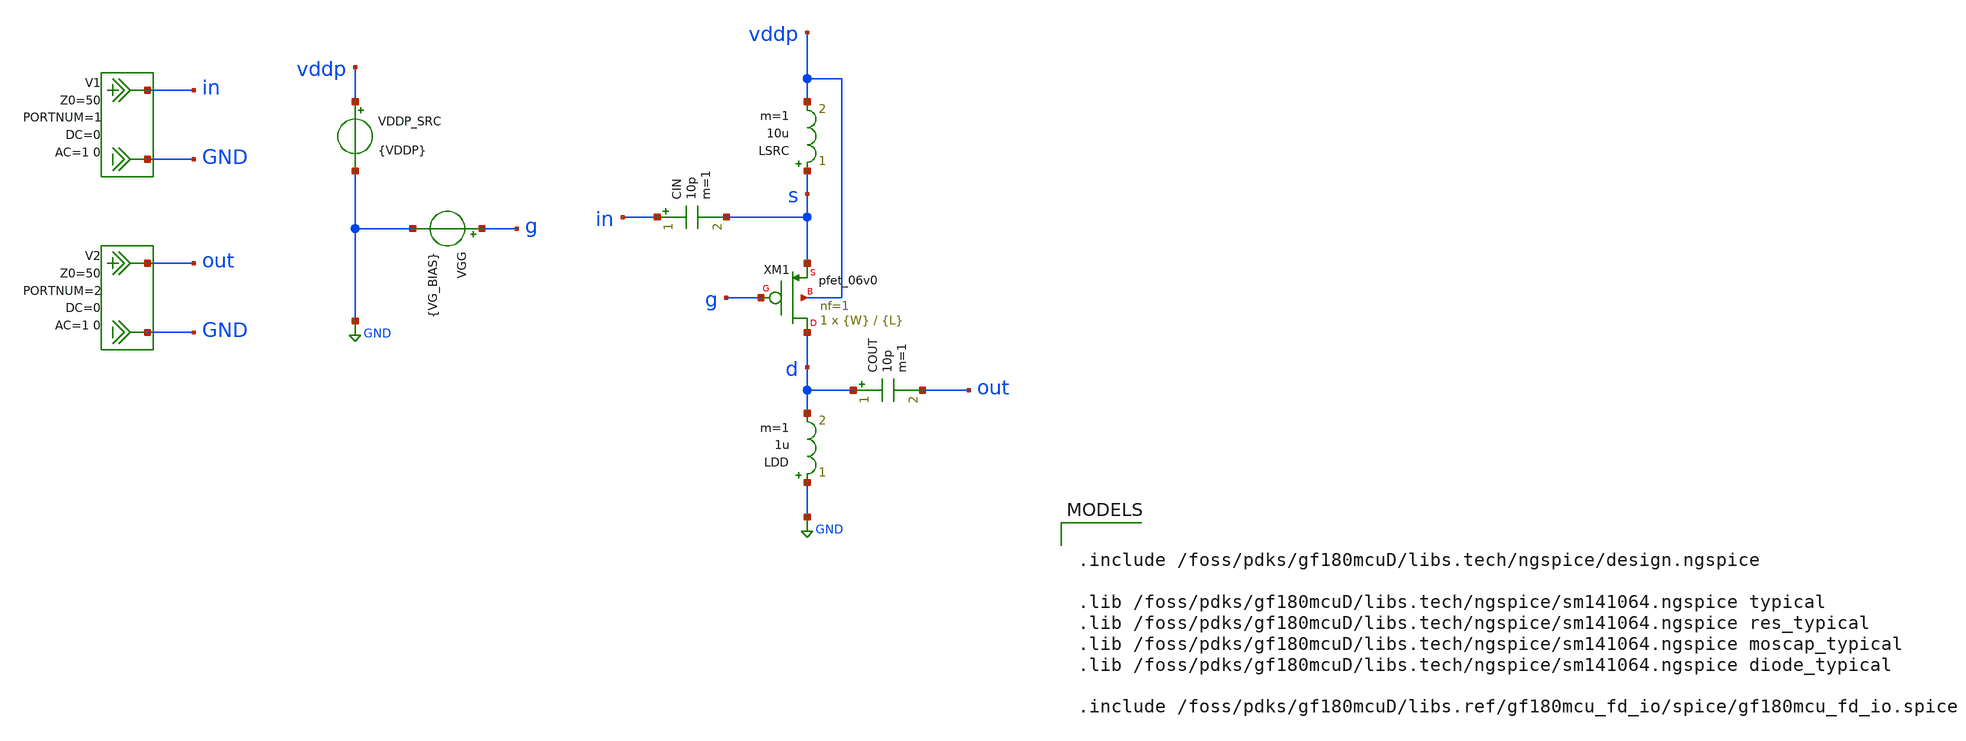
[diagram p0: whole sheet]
** sch_path: NFmin_Simulation/simulations/06v0/nfmin_jd_pmos_cg_06.sch
**.subckt nfmin_jd_pmos_cg_06
VGG g GND {VG_BIAS}
VDDP_SRC vddp GND {VDDP}
LDD GND d 1u m=1
COUT d out 10p m=1
CIN in s 10p m=1
V1 in GND DC 0 AC 1 0 portnum 1 z0 50
V2 out GND DC 0 AC 1 0 portnum 2 z0 50
LSRC s vddp 10u m=1
XM1 d g s vddp pfet_06v0 L={L} W={W} nf=1 ad='int((nf+1)/2) * W/nf * 0.18u' as='int((nf+2)/2) * W/nf * 0.18u'
+ pd='2*int((nf+1)/2) * (W/nf + 0.18u)' ps='2*int((nf+2)/2) * (W/nf + 0.18u)' nrd='0.18u / W' nrs='0.18u / W'
+ sa=0 sb=0 sd=0 m=1
**** begin user architecture code

.include /foss/pdks/gf180mcuD/libs.tech/ngspice/design.ngspice

.lib /foss/pdks/gf180mcuD/libs.tech/ngspice/sm141064.ngspice typical
.lib /foss/pdks/gf180mcuD/libs.tech/ngspice/sm141064.ngspice res_typical
.lib /foss/pdks/gf180mcuD/libs.tech/ngspice/sm141064.ngspice moscap_typical
.lib /foss/pdks/gf180mcuD/libs.tech/ngspice/sm141064.ngspice diode_typical

.include /foss/pdks/gf180mcuD/libs.ref/gf180mcu_fd_io/spice/gf180mcu_fd_io.spice




.option savecurrents

.param fnoicor=0
.param sw_stat_mismatch=0

* ============================================================
* Common-gate pfet_06v0 characterization
*
* Testbench:
*   VDDP_SRC vddp GND {VDDP}
*   LSRC s vddp 10u
*   XM1 d g s vddp pfet_06v0 ...
*
* Therefore:
*   Source DC ≈ VDDP
*   Drain DC  ≈ 0 V
*   VSD       ≈ VDDP
*   Gate DC   = VDDP - VSG_BIAS
*   VSG       ≈ VSG_BIAS
*
* Main chip-realistic / IO-compatible point: VDDP = 5.0 V
* 5.5 V checks upper IO supply margin.
* 6.0 V is device-only characterization.
* ============================================================

.param VDDP=5.0
.param VSG_BIAS=0.9
.param VG_BIAS={VDDP-VSG_BIAS}

* pfet_06v0 geometry defaults
.param W=0.30e-6
.param L=0.55e-6

.control
  set noaskquit
  save all

  echo VSD_V W_m L_m VSG_V ID_A JD_mA_per_um > pmos06_cg_geom_jd_dense.txt
  echo VSD_V W_m L_m VSG_V NFmin_dB NF_dB Rn_Ohm SOpt_real SOpt_imag > pmos06_cg_geom_nf_dense.txt

  * VDDP / VSD sweep:
  * 3.3 V  : low-voltage comparison
  * 5.0 V  : recommended nominal chip / IO-compatible point
  * 5.5 V  : upper IO operating check
  * 6.0 V  : 6 V device-only characterization point
  foreach vddpval 3.3 5.0 5.5 6.0

    * Width sweep in meters
    foreach wval 0.30e-6 1e-6 5e-6 10e-6 20e-6 50e-6

      * Length sweep in meters
      foreach lval 0.55e-6 0.70e-6 1.00e-6

        * VSG sweep:
        * 0.50 V to 2.50 V in 5 mV steps
        let vsg = 0.50

        while vsg le 2.5001

          alterparam VDDP = $vddpval
          alterparam W = $wval
          alterparam L = $lval
          alterparam VSG_BIAS = $&vsg
          reset

          op

          let idp_op = abs(i(vddp_src))
          let jd_p_op = 1e-3*idp_op/$wval

          echo $vddpval $wval $lval $&vsg $&idp_op $&jd_p_op >> pmos06_cg_geom_jd_dense.txt

          sp lin 1 2.4e9 2.4e9 1

          let nfmin_val = real(NFmin)
          let nf_val = real(NF)
          let rn_val = real(Rn)
          let sopt_re = real(SOpt)
          let sopt_im = imag(SOpt)

          echo $vddpval $wval $lval $&vsg $&nfmin_val $&nf_val $&rn_val $&sopt_re $&sopt_im >>
+ pmos06_cg_geom_nf_dense.txt

          let vsg = vsg + 0.005

        end

      end

    end

  end

.endc



**** end user architecture code
**.ends
.GLOBAL GND
.end
